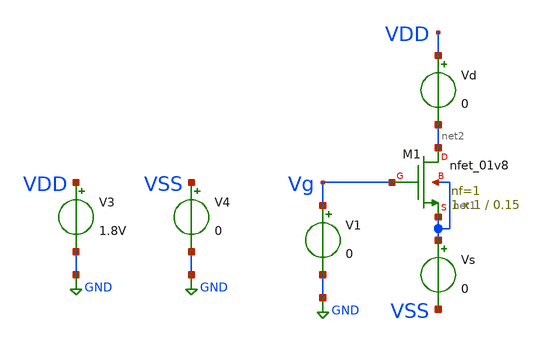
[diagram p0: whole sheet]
** sch_path: xschem/tests/dummy.sch
**.subckt dummy
V3 VDD GND 1.8V
V4 VSS GND 0
XM1 net2 Vg net1 net1 sky130_fd_pr__nfet_01v8 L=0.15 W=1 nf=1 ad='int((nf+1)/2) * W/nf * 0.29' as='int((nf+2)/2) * W/nf * 0.29'
+ pd='2*int((nf+1)/2) * (W/nf + 0.29)' ps='2*int((nf+2)/2) * (W/nf + 0.29)' nrd='0.29 / W' nrs='0.29 / W'
+ sa=0 sb=0 sd=0 mult=1 m=1
V1 Vg GND 0
Vd VDD net2 0
Vs net1 VSS 0
**** begin user architecture code
 .lib $::SKYWATER_MODELS/sky130.lib.spice tt
.include $::SKYWATER_STDCELLS/sky130_fd_sc_hd.spice


.options acct list
.temp 25
*vvcc VDD 0 dc 1.8
*vvss VSS 0 0
.control
*tran 0.1u 400u
dc v1 0 1.8V 0.1
*plot RST_PLS clk+2 Pulse+4
plot Vg-Vss
plot i(Vs)
write pulse_generator_test.raw
.endc


**** end user architecture code
**.ends
.GLOBAL GND
.end
